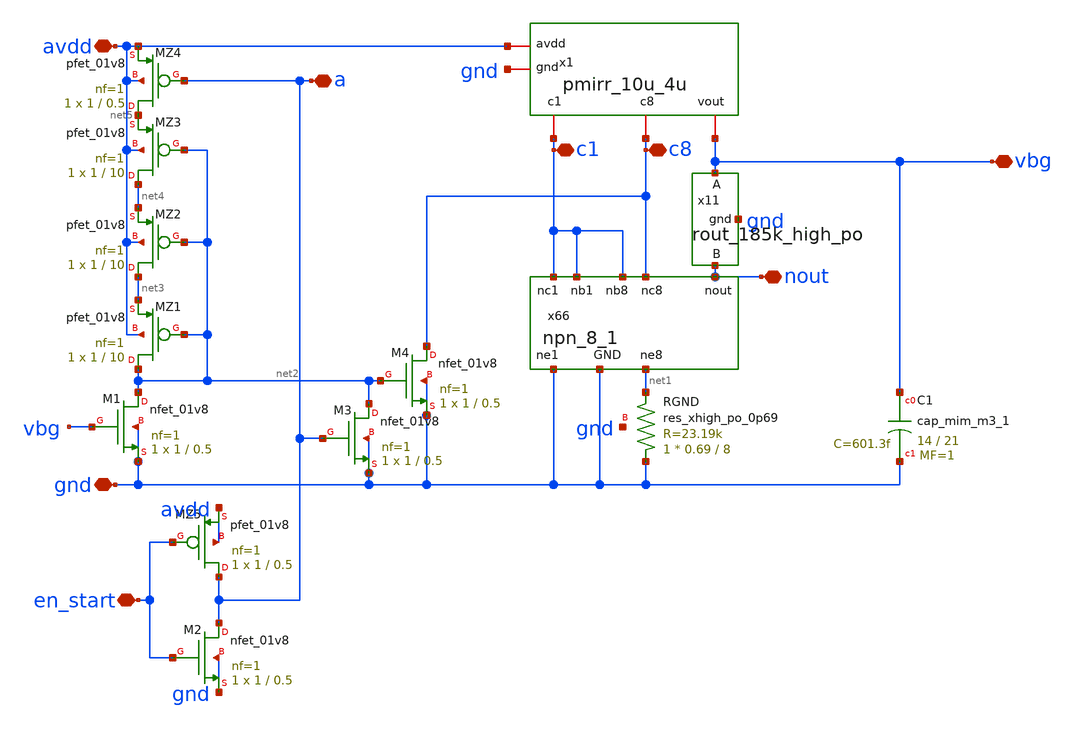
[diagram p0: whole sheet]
** sch_path: xschem/rev_1/tt_um_ik_0_ptat_bgr_core.sch
**.subckt tt_um_ik_0_ptat_bgr_core avdd gnd vbg en_start a c1 c8 nout
*.iopin avdd
*.iopin gnd
*.iopin vbg
*.iopin en_start
*.iopin a
*.iopin c1
*.iopin c8
*.iopin nout
XRGND gnd net1 gnd sky130_fd_pr__res_xhigh_po_0p69 L=8 mult=1 m=1
x1 avdd vbg c1 c8 gnd pmirr_10u_4u
x66 c1 c1 c1 c8 gnd gnd nout net1 npn_8_1
XMZ1 net2 net2 net3 avdd sky130_fd_pr__pfet_01v8 L=10 W=1 nf=1 ad='int((nf+1)/2) * W/nf * 0.29' as='int((nf+2)/2) * W/nf * 0.29'
+ pd='2*int((nf+1)/2) * (W/nf + 0.29)' ps='2*int((nf+2)/2) * (W/nf + 0.29)' nrd='0.29 / W' nrs='0.29 / W'
+ sa=0 sb=0 sd=0 mult=1 m=1
XMZ2 net3 net2 net4 avdd sky130_fd_pr__pfet_01v8 L=10 W=1 nf=1 ad='int((nf+1)/2) * W/nf * 0.29' as='int((nf+2)/2) * W/nf * 0.29'
+ pd='2*int((nf+1)/2) * (W/nf + 0.29)' ps='2*int((nf+2)/2) * (W/nf + 0.29)' nrd='0.29 / W' nrs='0.29 / W'
+ sa=0 sb=0 sd=0 mult=1 m=1
XMZ3 net4 net2 net5 avdd sky130_fd_pr__pfet_01v8 L=10 W=1 nf=1 ad='int((nf+1)/2) * W/nf * 0.29' as='int((nf+2)/2) * W/nf * 0.29'
+ pd='2*int((nf+1)/2) * (W/nf + 0.29)' ps='2*int((nf+2)/2) * (W/nf + 0.29)' nrd='0.29 / W' nrs='0.29 / W'
+ sa=0 sb=0 sd=0 mult=1 m=1
XMZ4 net5 a avdd avdd sky130_fd_pr__pfet_01v8 L=0.5 W=1 nf=1 ad='int((nf+1)/2) * W/nf * 0.29' as='int((nf+2)/2) * W/nf * 0.29'
+ pd='2*int((nf+1)/2) * (W/nf + 0.29)' ps='2*int((nf+2)/2) * (W/nf + 0.29)' nrd='0.29 / W' nrs='0.29 / W'
+ sa=0 sb=0 sd=0 mult=1 m=1
XMZ5 a en_start avdd avdd sky130_fd_pr__pfet_01v8 L=0.5 W=1 nf=1 ad='int((nf+1)/2) * W/nf * 0.29' as='int((nf+2)/2) * W/nf * 0.29'
+ pd='2*int((nf+1)/2) * (W/nf + 0.29)' ps='2*int((nf+2)/2) * (W/nf + 0.29)' nrd='0.29 / W' nrs='0.29 / W'
+ sa=0 sb=0 sd=0 mult=1 m=1
x11 vbg gnd nout rout_185k_high_po
XM2 a en_start gnd gnd sky130_fd_pr__nfet_01v8 L=0.5 W=1 nf=1 ad='int((1 + 1)/2) * 1 / 1 * 0.29' as='int((1 + 2)/2) * 1 / 1 * 0.29'
+ pd='2*int((1 + 1)/2) * (1 / 1 + 0.29)' ps='2*int((1 + 2)/2) * (1 / 1 + 0.29)' nrd='0.29 / 1 ' nrs='0.29 / 1 '
+ sa=0 sb=0 sd=0 mult=1 m=1
XM1 net2 vbg gnd gnd sky130_fd_pr__nfet_01v8 L=0.5 W=1 nf=1 ad='int((1 + 1)/2) * 1 / 1 * 0.29' as='int((1 + 2)/2) * 1 / 1 * 0.29'
+ pd='2*int((1 + 1)/2) * (1 / 1 + 0.29)' ps='2*int((1 + 2)/2) * (1 / 1 + 0.29)' nrd='0.29 / 1 ' nrs='0.29 / 1 '
+ sa=0 sb=0 sd=0 mult=1 m=1
XM3 net2 a gnd gnd sky130_fd_pr__nfet_01v8 L=0.5 W=1 nf=1 ad='int((1 + 1)/2) * 1 / 1 * 0.29' as='int((1 + 2)/2) * 1 / 1 * 0.29'
+ pd='2*int((1 + 1)/2) * (1 / 1 + 0.29)' ps='2*int((1 + 2)/2) * (1 / 1 + 0.29)' nrd='0.29 / 1 ' nrs='0.29 / 1 '
+ sa=0 sb=0 sd=0 mult=1 m=1
XM4 c8 net2 gnd gnd sky130_fd_pr__nfet_01v8 L=0.5 W=1 nf=1 ad='int((1 + 1)/2) * 1 / 1 * 0.29' as='int((1 + 2)/2) * 1 / 1 * 0.29'
+ pd='2*int((1 + 1)/2) * (1 / 1 + 0.29)' ps='2*int((1 + 2)/2) * (1 / 1 + 0.29)' nrd='0.29 / 1 ' nrs='0.29 / 1 '
+ sa=0 sb=0 sd=0 mult=1 m=1
XC1 vbg gnd sky130_fd_pr__cap_mim_m3_1 W=14 L=21 MF=1 m=1
**.ends
.end
